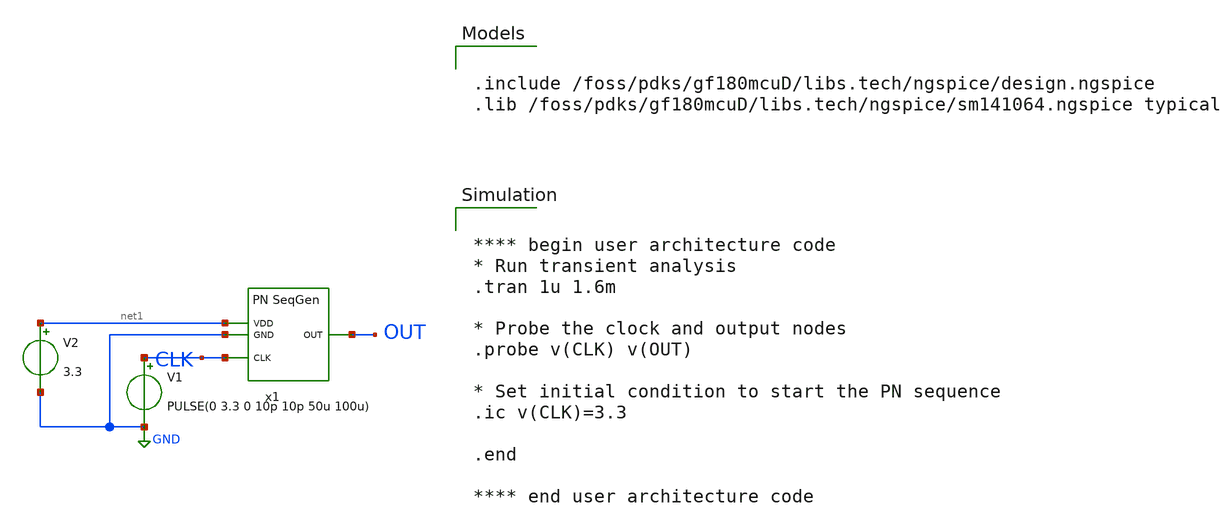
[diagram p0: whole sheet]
** sch_path: Project/1-on-chip/schematic/PNgen/tb_pn.sch
**.subckt tb_pn
V1 CLK GND PULSE(0 3.3 0 10p 10p 50u 100u)
V2 net1 GND 3.3
x1 net1 GND CLK OUT pn_8
**** begin user architecture code

.include /foss/pdks/gf180mcuD/libs.tech/ngspice/design.ngspice
.lib /foss/pdks/gf180mcuD/libs.tech/ngspice/sm141064.ngspice typical



**** begin user architecture code
* Run transient analysis
.tran 1u 1.6m

* Probe the clock and output nodes
.probe v(CLK) v(OUT)

* Set initial condition to start the PN sequence
.ic v(CLK)=3.3

.end

**** end user architecture code


**** end user architecture code
**.ends

* expanding   symbol:  pn_8.sym # of pins=4
** sym_path: Project/1-on-chip/schematic/PNgen/pn_8.sym
** sch_path: Project/1-on-chip/schematic/PNgen/pn_8.sch
.subckt pn_8 VDD GND CLK OUT
*.ipin VDD
*.ipin GND
*.ipin CLK
*.opin OUT
x1 net4 OUT VDD GND net3 xor
x2 VDD GND net3 CLK net1 net5 dff
x3 VDD GND net1 CLK net2 net6 dff
x4 VDD GND net2 CLK net4 net7 dff
x5 VDD GND net4 CLK OUT net8 dff
.ends


* expanding   symbol:  xor.sym # of pins=5
** sym_path: Project/1-on-chip/schematic/PNgen/xor.sym
** sch_path: Project/1-on-chip/schematic/PNgen/xor.sch
.subckt xor A B VDD VSS OUT
*.ipin VDD
*.opin OUT
*.ipin A
*.ipin B
*.ipin VSS
XM7 OUT net2 net4 net4 pfet_03v3 L=0.28u W=1.3u nf=1 ad='int((nf+1)/2) * W/nf * 0.18u' as='int((nf+2)/2) * W/nf * 0.18u'
+ pd='2*int((nf+1)/2) * (W/nf + 0.18u)' ps='2*int((nf+2)/2) * (W/nf + 0.18u)' nrd='0.18u / W' nrs='0.18u / W'
+ sa=0 sb=0 sd=0 m=1
XM1 VDD B net4 VDD pfet_03v3 L=0.28u W=1.3u nf=1 ad='int((nf+1)/2) * W/nf * 0.18u' as='int((nf+2)/2) * W/nf * 0.18u'
+ pd='2*int((nf+1)/2) * (W/nf + 0.18u)' ps='2*int((nf+2)/2) * (W/nf + 0.18u)' nrd='0.18u / W' nrs='0.18u / W'
+ sa=0 sb=0 sd=0 m=1
XM2 net1 A OUT net1 nfet_03v3 L=0.28u W=0.6u nf=1 ad='int((nf+1)/2) * W/nf * 0.18u' as='int((nf+2)/2) * W/nf * 0.18u'
+ pd='2*int((nf+1)/2) * (W/nf + 0.18u)' ps='2*int((nf+2)/2) * (W/nf + 0.18u)' nrd='0.18u / W' nrs='0.18u / W'
+ sa=0 sb=0 sd=0 m=1
XM8 VSS B net1 VSS nfet_03v3 L=0.28u W=0.6u nf=1 ad='int((nf+1)/2) * W/nf * 0.18u' as='int((nf+2)/2) * W/nf * 0.18u'
+ pd='2*int((nf+1)/2) * (W/nf + 0.18u)' ps='2*int((nf+2)/2) * (W/nf + 0.18u)' nrd='0.18u / W' nrs='0.18u / W'
+ sa=0 sb=0 sd=0 m=1
XM9 OUT net2 VSS VSS nfet_03v3 L=0.28u W=0.6u nf=1 ad='int((nf+1)/2) * W/nf * 0.18u' as='int((nf+2)/2) * W/nf * 0.18u'
+ pd='2*int((nf+1)/2) * (W/nf + 0.18u)' ps='2*int((nf+2)/2) * (W/nf + 0.18u)' nrd='0.18u / W' nrs='0.18u / W'
+ sa=0 sb=0 sd=0 m=1
XM10 net2 A VSS VSS nfet_03v3 L=0.28u W=0.6u nf=1 ad='int((nf+1)/2) * W/nf * 0.18u' as='int((nf+2)/2) * W/nf * 0.18u'
+ pd='2*int((nf+1)/2) * (W/nf + 0.18u)' ps='2*int((nf+2)/2) * (W/nf + 0.18u)' nrd='0.18u / W' nrs='0.18u / W'
+ sa=0 sb=0 sd=0 m=1
XM11 VSS B net2 VSS nfet_03v3 L=0.28u W=0.6u nf=1 ad='int((nf+1)/2) * W/nf * 0.18u' as='int((nf+2)/2) * W/nf * 0.18u'
+ pd='2*int((nf+1)/2) * (W/nf + 0.18u)' ps='2*int((nf+2)/2) * (W/nf + 0.18u)' nrd='0.18u / W' nrs='0.18u / W'
+ sa=0 sb=0 sd=0 m=1
XM3 net4 A VDD VDD pfet_03v3 L=0.28u W=1.3u nf=1 ad='int((nf+1)/2) * W/nf * 0.18u' as='int((nf+2)/2) * W/nf * 0.18u'
+ pd='2*int((nf+1)/2) * (W/nf + 0.18u)' ps='2*int((nf+2)/2) * (W/nf + 0.18u)' nrd='0.18u / W' nrs='0.18u / W'
+ sa=0 sb=0 sd=0 m=1
XM4 net3 A VDD VDD pfet_03v3 L=0.28u W=1.3u nf=1 ad='int((nf+1)/2) * W/nf * 0.18u' as='int((nf+2)/2) * W/nf * 0.18u'
+ pd='2*int((nf+1)/2) * (W/nf + 0.18u)' ps='2*int((nf+2)/2) * (W/nf + 0.18u)' nrd='0.18u / W' nrs='0.18u / W'
+ sa=0 sb=0 sd=0 m=1
XM5 net2 B net3 net3 pfet_03v3 L=0.28u W=1.3u nf=1 ad='int((nf+1)/2) * W/nf * 0.18u' as='int((nf+2)/2) * W/nf * 0.18u'
+ pd='2*int((nf+1)/2) * (W/nf + 0.18u)' ps='2*int((nf+2)/2) * (W/nf + 0.18u)' nrd='0.18u / W' nrs='0.18u / W'
+ sa=0 sb=0 sd=0 m=1
.ends


* expanding   symbol:  dff.sym # of pins=6
** sym_path: Project/1-on-chip/schematic/PNgen/dff.sym
** sch_path: Project/1-on-chip/schematic/PNgen/dff.sch
.subckt dff VDD GND D CLK Q Qbar
*.ipin VDD
*.opin Q
*.ipin GND
*.ipin D
*.ipin CLK
*.opin Qbar
XM9 D CLK net3 net3 nfet_03v3 L=0.28u W=0.34u nf=1 ad='int((nf+1)/2) * W/nf * 0.18u' as='int((nf+2)/2) * W/nf * 0.18u'
+ pd='2*int((nf+1)/2) * (W/nf + 0.18u)' ps='2*int((nf+2)/2) * (W/nf + 0.18u)' nrd='0.18u / W' nrs='0.18u / W'
+ sa=0 sb=0 sd=0 m=1
XM2 net4 CLK Q Q nfet_03v3 L=0.28u W=0.34u nf=1 ad='int((nf+1)/2) * W/nf * 0.18u' as='int((nf+2)/2) * W/nf * 0.18u'
+ pd='2*int((nf+1)/2) * (W/nf + 0.18u)' ps='2*int((nf+2)/2) * (W/nf + 0.18u)' nrd='0.18u / W' nrs='0.18u / W'
+ sa=0 sb=0 sd=0 m=1
XM6 net1 net3 GND GND nfet_03v3 L=0.28u W=0.34u nf=1 ad='int((nf+1)/2) * W/nf * 0.18u' as='int((nf+2)/2) * W/nf * 0.18u'
+ pd='2*int((nf+1)/2) * (W/nf + 0.18u)' ps='2*int((nf+2)/2) * (W/nf + 0.18u)' nrd='0.18u / W' nrs='0.18u / W'
+ sa=0 sb=0 sd=0 m=1
XM8 net2 net1 GND GND nfet_03v3 L=0.28u W=0.34u nf=1 ad='int((nf+1)/2) * W/nf * 0.18u' as='int((nf+2)/2) * W/nf * 0.18u'
+ pd='2*int((nf+1)/2) * (W/nf + 0.18u)' ps='2*int((nf+2)/2) * (W/nf + 0.18u)' nrd='0.18u / W' nrs='0.18u / W'
+ sa=0 sb=0 sd=0 m=1
XM10 Qbar net4 GND GND nfet_03v3 L=0.28u W=0.34u nf=1 ad='int((nf+1)/2) * W/nf * 0.18u' as='int((nf+2)/2) * W/nf * 0.18u'
+ pd='2*int((nf+1)/2) * (W/nf + 0.18u)' ps='2*int((nf+2)/2) * (W/nf + 0.18u)' nrd='0.18u / W' nrs='0.18u / W'
+ sa=0 sb=0 sd=0 m=1
XM13 Q Qbar GND GND nfet_03v3 L=0.28u W=0.34u nf=1 ad='int((nf+1)/2) * W/nf * 0.18u' as='int((nf+2)/2) * W/nf * 0.18u'
+ pd='2*int((nf+1)/2) * (W/nf + 0.18u)' ps='2*int((nf+2)/2) * (W/nf + 0.18u)' nrd='0.18u / W' nrs='0.18u / W'
+ sa=0 sb=0 sd=0 m=1
XM1 net1 net3 VDD VDD pfet_03v3 L=0.28u W=0.85u nf=1 ad='int((nf+1)/2) * W/nf * 0.18u' as='int((nf+2)/2) * W/nf * 0.18u'
+ pd='2*int((nf+1)/2) * (W/nf + 0.18u)' ps='2*int((nf+2)/2) * (W/nf + 0.18u)' nrd='0.18u / W' nrs='0.18u / W'
+ sa=0 sb=0 sd=0 m=1
XM3 net2 net1 VDD VDD pfet_03v3 L=0.28u W=0.85u nf=1 ad='int((nf+1)/2) * W/nf * 0.18u' as='int((nf+2)/2) * W/nf * 0.18u'
+ pd='2*int((nf+1)/2) * (W/nf + 0.18u)' ps='2*int((nf+2)/2) * (W/nf + 0.18u)' nrd='0.18u / W' nrs='0.18u / W'
+ sa=0 sb=0 sd=0 m=1
XM5 Qbar net4 VDD VDD pfet_03v3 L=0.28u W=0.85u nf=1 ad='int((nf+1)/2) * W/nf * 0.18u' as='int((nf+2)/2) * W/nf * 0.18u'
+ pd='2*int((nf+1)/2) * (W/nf + 0.18u)' ps='2*int((nf+2)/2) * (W/nf + 0.18u)' nrd='0.18u / W' nrs='0.18u / W'
+ sa=0 sb=0 sd=0 m=1
XM7 Q Qbar VDD VDD pfet_03v3 L=0.28u W=0.85u nf=1 ad='int((nf+1)/2) * W/nf * 0.18u' as='int((nf+2)/2) * W/nf * 0.18u'
+ pd='2*int((nf+1)/2) * (W/nf + 0.18u)' ps='2*int((nf+2)/2) * (W/nf + 0.18u)' nrd='0.18u / W' nrs='0.18u / W'
+ sa=0 sb=0 sd=0 m=1
XM11 net2 CLK net3 net3 pfet_03v3 L=0.28u W=0.85u nf=1 ad='int((nf+1)/2) * W/nf * 0.18u' as='int((nf+2)/2) * W/nf * 0.18u'
+ pd='2*int((nf+1)/2) * (W/nf + 0.18u)' ps='2*int((nf+2)/2) * (W/nf + 0.18u)' nrd='0.18u / W' nrs='0.18u / W'
+ sa=0 sb=0 sd=0 m=1
XM12 net4 CLK net2 net2 pfet_03v3 L=0.28u W=0.85u nf=1 ad='int((nf+1)/2) * W/nf * 0.18u' as='int((nf+2)/2) * W/nf * 0.18u'
+ pd='2*int((nf+1)/2) * (W/nf + 0.18u)' ps='2*int((nf+2)/2) * (W/nf + 0.18u)' nrd='0.18u / W' nrs='0.18u / W'
+ sa=0 sb=0 sd=0 m=1
.ends

.GLOBAL GND
.end
